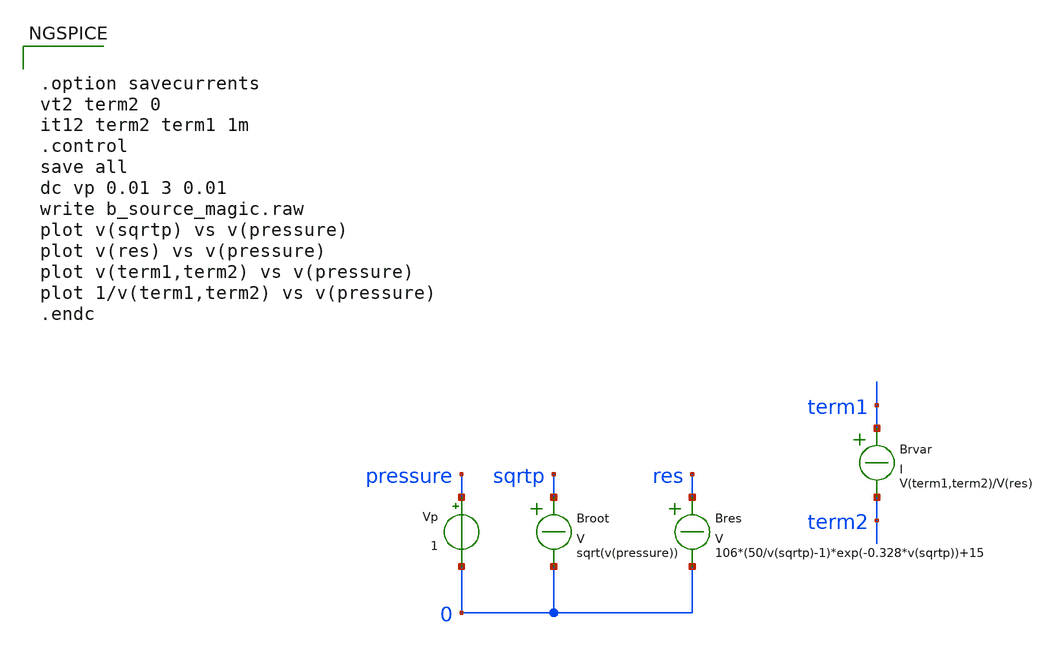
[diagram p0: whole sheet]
** sch_path: sensormodels/b_source_magic.sch
* Copyright 2020 Stefan Frederik Schippers
* Licensed under the Apache License, Version 2.0 (the "License");
* you may not use this file except in compliance with the License.
* You may obtain a copy of the License at
* https://www.apache.org/licenses/LICENSE-2.0
* Unless required by applicable law or agreed to in writing, software
* distributed under the License is distributed on an "AS IS" BASIS,
* WITHOUT WARRANTIES OR CONDITIONS OF ANY KIND, either express or implied.
* See the License for the specific language governing permissions and
* limitations under the License.
**.subckt b_source_magic
Broot sqrtp 0 V = sqrt(v(pressure))
Vp pressure 0 1
Bres res 0 V = 106*(50/v(sqrtp)-1)*exp(-0.328*v(sqrtp))+15
Brvar term1 term2 I = V(term1,term2)/V(res)
**** begin user architecture code


.option savecurrents
vt2 term2 0
it12 term2 term1 1m
.control
save all
dc vp 0.01 3 0.01
write b_source_magic.raw
plot v(sqrtp) vs v(pressure)
plot v(res) vs v(pressure)
plot v(term1,term2) vs v(pressure)
plot 1/v(term1,term2) vs v(pressure)
.endc


**** end user architecture code
**.ends
.end
